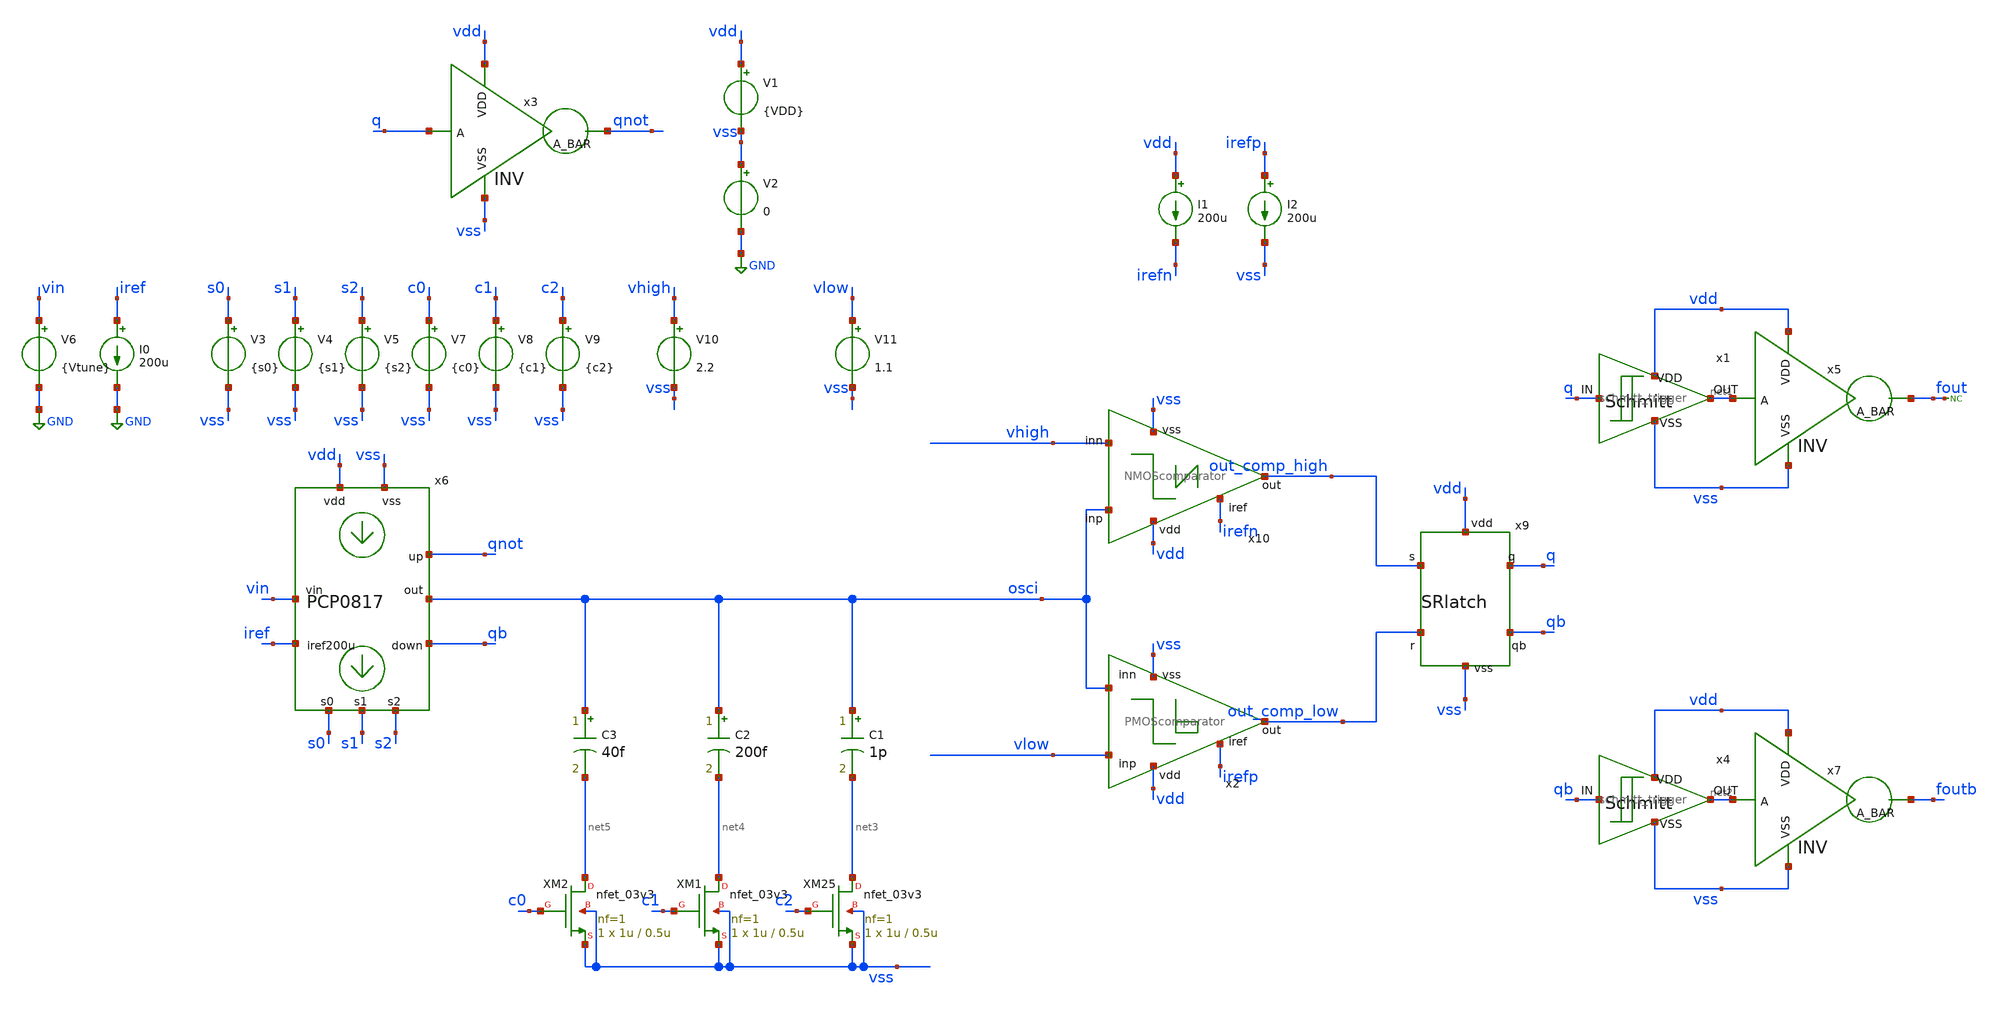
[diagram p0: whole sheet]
** sch_path: designs/libs/qw_core_analog_pkedit/VCO0817/VCO0817.sch
**.subckt VCO0817
V1 vdd vss {VDD}
V2 vss GND 0
C1 osci net3 1p m=1
I1 vdd irefn 200u
I2 irefp vss 200u
x9 vdd out_comp_high q qb out_comp_low vss SRlatch
x2 vdd irefp vlow out_comp_low osci vss PMOScomparator
x10 vdd osci out_comp_high vhigh irefn vss NMOScomparator
x3 vdd q qnot vss INV
x1 q net1 vdd vss schmitt_trigger
x4 qb net2 vdd vss schmitt_trigger
x5 vdd net1 fout vss INV
x7 vdd net2 foutb vss INV
V6 vin GND {Vtune}
I0 iref GND 200u
* noconn fout
x6 vdd vss vin iref osci qnot qb s0 s1 s2 PCP0817
V3 s0 vss {s0}
V4 s1 vss {s1}
V5 s2 vss {s2}
XM25 net3 c2 vss vss nfet_03v3 L=0.5u W=1u nf=1 ad='int((nf+1)/2) * W/nf * 0.18u' as='int((nf+2)/2) * W/nf * 0.18u'
+ pd='2*int((nf+1)/2) * (W/nf + 0.18u)' ps='2*int((nf+2)/2) * (W/nf + 0.18u)' nrd='0.18u / W' nrs='0.18u / W'
+ sa=0 sb=0 sd=0 m=1
XM1 net4 c1 vss vss nfet_03v3 L=0.5u W=1u nf=1 ad='int((nf+1)/2) * W/nf * 0.18u' as='int((nf+2)/2) * W/nf * 0.18u'
+ pd='2*int((nf+1)/2) * (W/nf + 0.18u)' ps='2*int((nf+2)/2) * (W/nf + 0.18u)' nrd='0.18u / W' nrs='0.18u / W'
+ sa=0 sb=0 sd=0 m=1
XM2 net5 c0 vss vss nfet_03v3 L=0.5u W=1u nf=1 ad='int((nf+1)/2) * W/nf * 0.18u' as='int((nf+2)/2) * W/nf * 0.18u'
+ pd='2*int((nf+1)/2) * (W/nf + 0.18u)' ps='2*int((nf+2)/2) * (W/nf + 0.18u)' nrd='0.18u / W' nrs='0.18u / W'
+ sa=0 sb=0 sd=0 m=1
V7 c0 vss {c0}
V8 c1 vss {c1}
V9 c2 vss {c2}
C2 osci net4 200f m=1
C3 osci net5 40f m=1
V10 vhigh vss 2.2
V11 vlow vss 1.1
**** begin user architecture code


* .param par_vth=0 par_k=0 par_l=0 par_w=0 par_leff=0 par_weff=0 p_sqrtarea=0 var_k=0 var_vth=0
.param VDD = 3.3
.param Vtune = 1.5
.param s0 = 3.3 s1 = 0 s2 = 0 c0 = 0 c1 = 0 c2 = 3.3
.control
save all

**OP
**show all > op.log
**show all

** Source settings
alter @V1[PULSE] = [ 0 3.3 5n 1n 1n 49.998u 100u 0 ]

** Simulation settings
* .step param Vtune 0 3.3 0.1
tran .1n 5u

.mea tran TPER TRIG fout VAL={VDD/2} RISE=1 FROM=5u  TARG fout VAL={VDD/2} RISE=2
.mea tran FREQ param='1/TPER'

write VCO0817.raw
.endc



.include $::180MCU_MODELS/design.ngspice
.lib $::180MCU_MODELS/sm141064.ngspice typical
.lib $::180MCU_MODELS/sm141064.ngspice cap_mim
.lib $::180MCU_MODELS/sm141064.ngspice res_typical
.lib $::180MCU_MODELS/sm141064.ngspice moscap_typical
.lib $::180MCU_MODELS/sm141064.ngspice mimcap_typical
* .lib $::180MCU_MODELS/sm141064.ngspice res_statistical

**** end user architecture code
**.ends
.GLOBAL GND
.end
